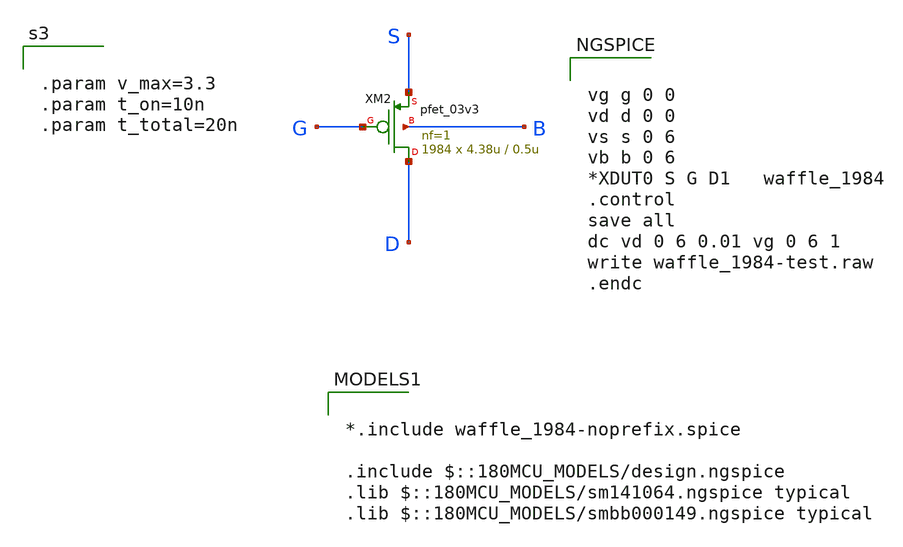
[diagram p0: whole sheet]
** sch_path: LDO/xschem/waffle_1984/waffle_1984-test.sch

.include $env(PDK_ROOT)/$env(PDK)/libs.tech/ngspice/design.ngspice
.lib $env(PDK_ROOT)/$env(PDK)/libs.tech/ngspice/sm141064.ngspice typical
.lib $env(PDK_ROOT)/$env(PDK)/libs.tech/ngspice/sm141064.ngspice mimcap_statistical
.lib $env(PDK_ROOT)/$env(PDK)/libs.tech/ngspice/sm141064.ngspice cap_mim
.lib $env(PDK_ROOT)/$env(PDK)/libs.tech/ngspice/sm141064.ngspice res_typical
.lib $env(PDK_ROOT)/$env(PDK)/libs.tech/ngspice/sm141064.ngspice bjt_typical
.lib $env(PDK_ROOT)/$env(PDK)/libs.tech/ngspice/sm141064.ngspice moscap_typical

**.subckt waffle_1984-test
XM2 D G S B pfet_03v3 L=0.5u W=4.38u nf=1 ad='int((nf+1)/2) * W/nf * 0.18u' as='int((nf+2)/2) * W/nf * 0.18u'
+ pd='2*int((nf+1)/2) * (W/nf + 0.18u)' ps='2*int((nf+2)/2) * (W/nf + 0.18u)' nrd='0.18u / W' nrs='0.18u / W'
+ sa=0 sb=0 sd=0 m=1984
**** begin user architecture code


.param v_max=3.3
.param t_on=10n
.param t_total=20n




vg g 0 0
vd d 0 0
vs s 0 6
vb b 0 6
*XDUT0 S G D1   waffle_1984
.control
save all
dc vd 0 6 0.01 vg 0 6 1
write waffle_1984-test.raw
.endc



*.include waffle_1984-noprefix.spice

.include $::180MCU_MODELS/design.ngspice
.lib $::180MCU_MODELS/sm141064.ngspice typical
.lib $::180MCU_MODELS/smbb000149.ngspice typical

**** end user architecture code
**.ends
.end
